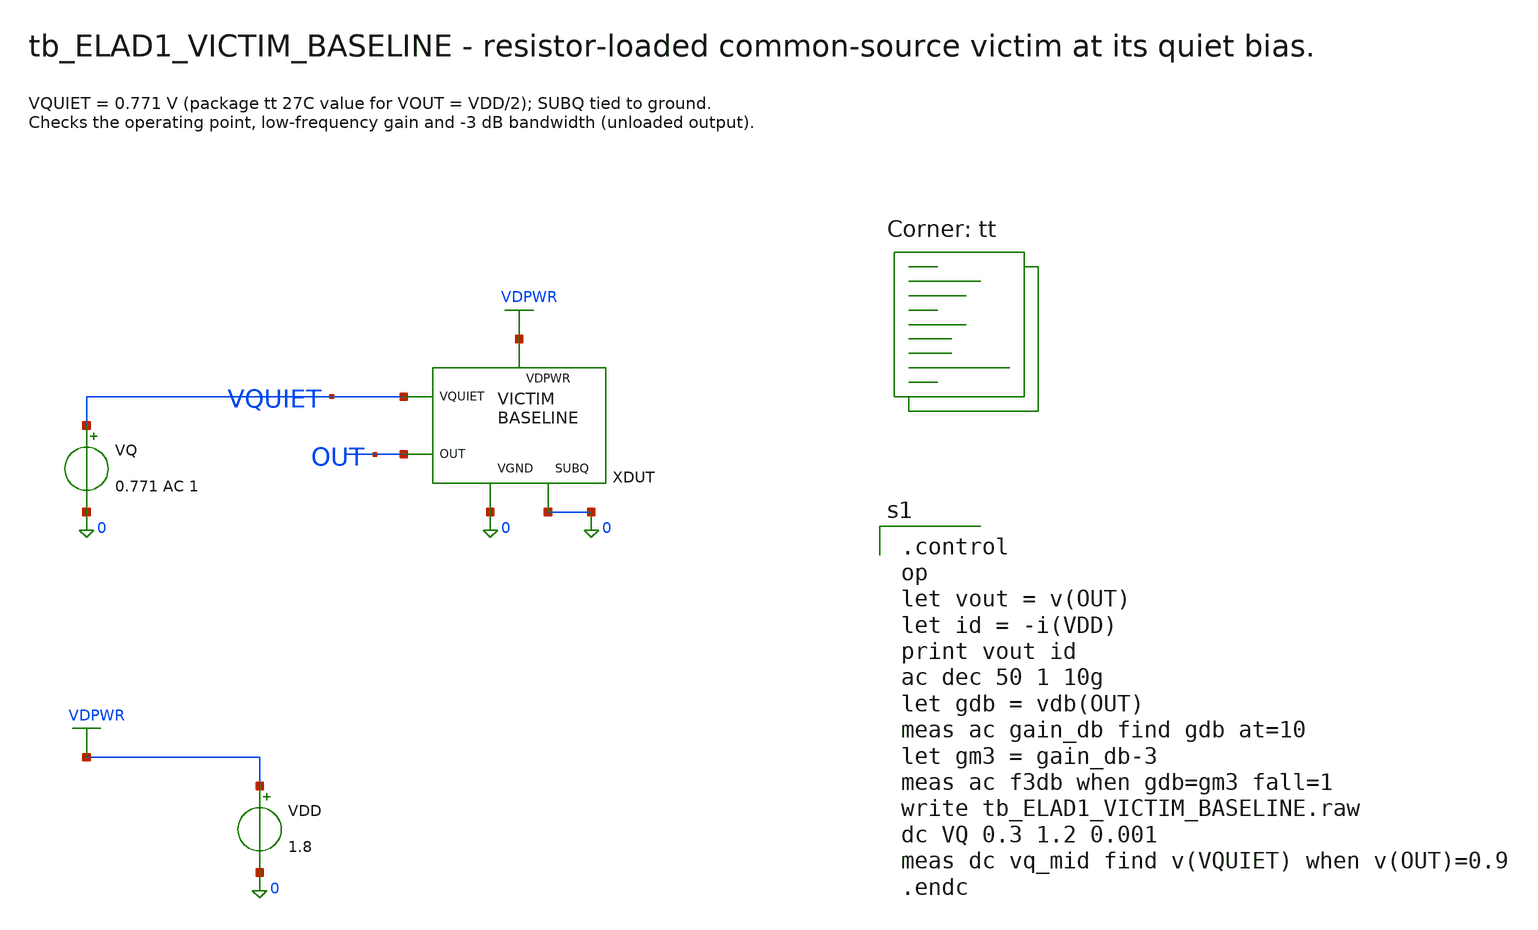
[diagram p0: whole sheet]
** sch_path: cells/ELAD1_VICTIM_BASELINE/schematic/tb_ELAD1_VICTIM_BASELINE.sch
**.subckt tb_ELAD1_VICTIM_BASELINE
XDUT VQUIET OUT VDPWR 0 0 ELAD1_VICTIM_BASELINE
VQ VQUIET 0 0.771 AC 1
VDD VDPWR 0 1.8
**** begin user architecture code

.control
op
let vout = v(OUT)
let id = -i(VDD)
print vout id
ac dec 50 1 10g
let gdb = vdb(OUT)
meas ac gain_db find gdb at=10
let gm3 = gain_db-3
meas ac f3db when gdb=gm3 fall=1
write tb_ELAD1_VICTIM_BASELINE.raw
dc VQ 0.3 1.2 0.001
meas dc vq_mid find v(VQUIET) when v(OUT)=0.9
.endc

.lib $::SKYWATER_MODELS/sky130.lib.spice tt
**** end user architecture code
**.ends

* expanding   symbol:  ELAD1_VICTIM_BASELINE.sym # of pins=5
** sym_path: cells/ELAD1_VICTIM_BASELINE/schematic/ELAD1_VICTIM_BASELINE.sym
** sch_path: cells/ELAD1_VICTIM_BASELINE/schematic/ELAD1_VICTIM_BASELINE.sch
.subckt ELAD1_VICTIM_BASELINE VQUIET OUT VDPWR VGND SUBQ
*.iopin VQUIET
*.iopin OUT
*.iopin VDPWR
*.iopin VGND
*.iopin SUBQ
XRLD VDPWR OUT SUBQ sky130_fd_pr__res_xhigh_po W=0.69 L=31.7 mult=1 m=1
XMVIC OUT VQUIET VGND SUBQ sky130_fd_pr__nfet_01v8 L=1 W=2 nf=1 ad='int((1 + 1)/2) * 2 / 1 * 0.29' as='int((1 + 2)/2) * 2 / 1 * 0.29'
+ pd='2*int((1 + 1)/2) * (2 / 1 + 0.29)' ps='2*int((1 + 2)/2) * (2 / 1 + 0.29)' nrd='0.29 / 2 ' nrs='0.29 / 2 '
+ sa=0 sb=0 sd=0 mult=1 m=1
XDUM[1] VGND VGND VGND SUBQ sky130_fd_pr__nfet_01v8 L=1 W=2 nf=1 ad='int((1 + 1)/2) * 2 / 1 * 0.29' as='int((1 + 2)/2) * 2 / 1 * 0.29'
+ pd='2*int((1 + 1)/2) * (2 / 1 + 0.29)' ps='2*int((1 + 2)/2) * (2 / 1 + 0.29)' nrd='0.29 / 2 ' nrs='0.29 / 2 '
+ sa=0 sb=0 sd=0 mult=1 m=1
XDUM[0] VGND VGND VGND SUBQ sky130_fd_pr__nfet_01v8 L=1 W=2 nf=1 ad='int((1 + 1)/2) * 2 / 1 * 0.29' as='int((1 + 2)/2) * 2 / 1 * 0.29'
+ pd='2*int((1 + 1)/2) * (2 / 1 + 0.29)' ps='2*int((1 + 2)/2) * (2 / 1 + 0.29)' nrd='0.29 / 2 ' nrs='0.29 / 2 '
+ sa=0 sb=0 sd=0 mult=1 m=1
.ends

.end
